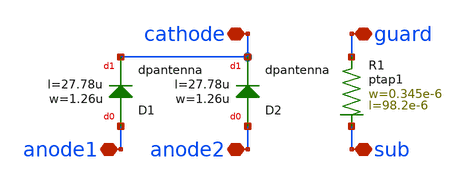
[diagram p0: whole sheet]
** sch_path: MSPHY6034-main/schematic/xschem/openpdk-libraries/ihp-sg13g2/sg13g2_io/xschem/sg13g2_DCPDiode.sch
**.subckt sg13g2_DCPDiode anode2 cathode guard anode1 sub
*.iopin anode2
*.iopin cathode
*.iopin guard
*.iopin anode1
*.iopin sub
XD1 anode1 cathode dpantenna l=27.78u w=1.26u
XR1 guard sub ptap1 R=4.243 w=0.345e-6 l=98.2e-6
XD2 anode2 cathode dpantenna l=27.78u w=1.26u
**.ends
.end
